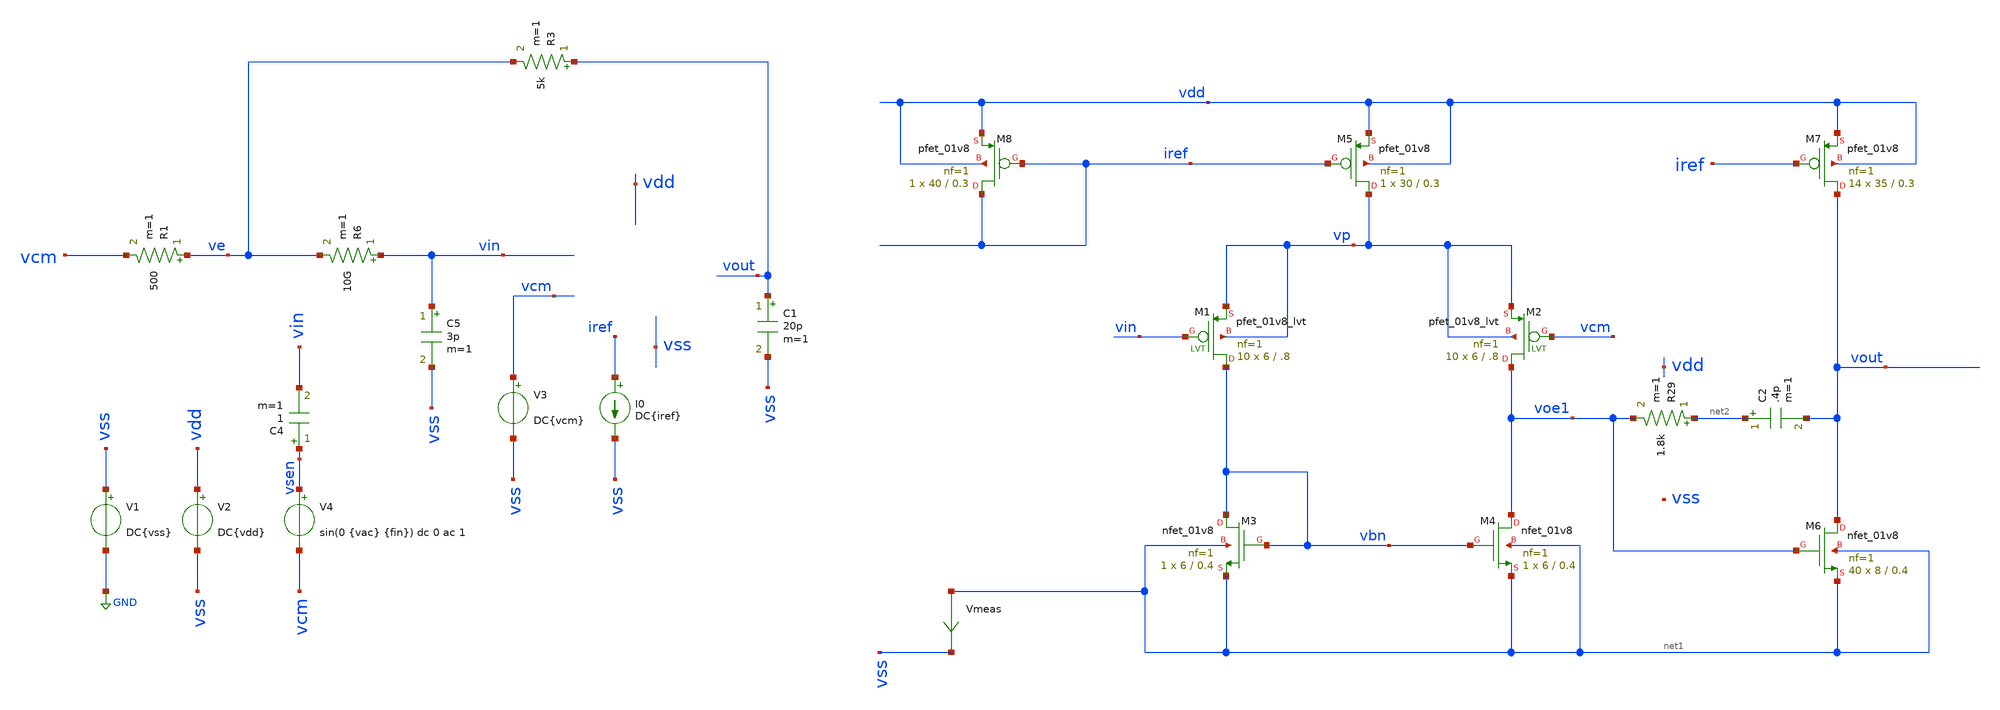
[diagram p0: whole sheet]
** sch_path: opamp/tb_opamp_openloop2.sch
**.subckt tb_opamp_openloop2
V1 vss GND DC{vss}
V2 vdd vss DC{vdd}
V3 vcm vss DC{vcm}
V4 vsen vcm sin(0 {vac} {fin}) dc 0 ac 1
C4 vsen vin 1 m=1
I0 iref vss DC{iref}
R1 ve vcm 500 m=1
R3 vout ve 5k m=1
C5 vin vss 3p m=1
C1 vout vss 20p m=1
R6 vin ve 10G m=1
XM3 vbn vbn net1 net1 sky130_fd_pr__nfet_01v8 L=0.4 W=6 nf=1 ad='W * 0.29' as='W * 0.29' pd='2 * (W + 0.29)'
+ ps='2 * (W + 0.29)' nrd='0.29 / W' nrs='0.29 / W' sa=0 sb=0 sd=0 mult=1 m=1
XM4 voe1 vbn net1 net1 sky130_fd_pr__nfet_01v8 L=0.4 W=6 nf=1 ad='W * 0.29' as='W * 0.29' pd='2 * (W + 0.29)'
+ ps='2 * (W + 0.29)' nrd='0.29 / W' nrs='0.29 / W' sa=0 sb=0 sd=0 mult=1 m=1
XM5 vp iref vdd vdd sky130_fd_pr__pfet_01v8 L=0.3 W=30 nf=1 ad='W * 0.29' as='W * 0.29' pd='2 * (W + 0.29)'
+ ps='2 * (W + 0.29)' nrd='0.29 / W' nrs='0.29 / W' sa=0 sb=0 sd=0 mult=1 m=1
XM7 vout iref vdd vdd sky130_fd_pr__pfet_01v8 L=0.3 W=35 nf=1 ad='W * 0.29' as='W * 0.29' pd='2 * (W + 0.29)'
+ ps='2 * (W + 0.29)' nrd='0.29 / W' nrs='0.29 / W' sa=0 sb=0 sd=0 mult=14 m=14
XM8 iref iref vdd vdd sky130_fd_pr__pfet_01v8 L=0.3 W=40 nf=1 ad='W * 0.29' as='W * 0.29' pd='2 * (W + 0.29)'
+ ps='2 * (W + 0.29)' nrd='0.29 / W' nrs='0.29 / W' sa=0 sb=0 sd=0 mult=1 m=1
XM6 vout voe1 net1 net1 sky130_fd_pr__nfet_01v8 L=0.4 W=8 nf=1 ad='W * 0.29' as='W * 0.29' pd='2 * (W + 0.29)'
+ ps='2 * (W + 0.29)' nrd='0.29 / W' nrs='0.29 / W' sa=0 sb=0 sd=0 mult=40 m=40
XM1 vbn vin vp vp sky130_fd_pr__pfet_01v8_lvt L=.8 W=6 nf=1 ad='int((nf+1)/2) * W/nf * 0.29' as='int((nf+2)/2) * W/nf * 0.29'
+ pd='2*int((nf+1)/2) * (W/nf + 0.29)' ps='2*int((nf+2)/2) * (W/nf + 0.29)' nrd='0.29 / W' nrs='0.29 / W'
+ sa=0 sb=0 sd=0 mult=10 m=10
XM2 voe1 vcm vp vp sky130_fd_pr__pfet_01v8_lvt L=.8 W=6 nf=1 ad='int((nf+1)/2) * W/nf * 0.29' as='int((nf+2)/2) * W/nf * 0.29'
+ pd='2*int((nf+1)/2) * (W/nf + 0.29)' ps='2*int((nf+2)/2) * (W/nf + 0.29)' nrd='0.29 / W' nrs='0.29 / W'
+ sa=0 sb=0 sd=0 mult=10 m=10
C2 net2 vout .4p m=1
Vmeas net1 vss 0
.save i(vmeas)
R29 net2 voe1 1.8k m=1
**** begin user architecture code




* Circuit Parameters
.param iref = 100u
.param vdd  = 1.8
.param vss  = 0.0
.param vcm  = 0.8
.param vac  = 10m
.param fin  = 9.765625e5
.options TEMP = 65.0

* Include Models
*.lib ~/skywater/skywater-pdk/libraries/sky130_fd_pr_ngspice/latest/models/corners/sky130.lib TT
*.lib /foss/pdks/sky130A/libs.tech/ngspice/sky130.lib.spice tt
.lib /foss/pdks/sky130A/libs.tech/ngspice/sky130.lib.spice.tt.red tt
* OP Parameters & Singals to save
.save all  @M.X1.XM1.msky130_fd_pr__pfet_01v8_lvt[id] @M.X1.XM1.msky130_fd_pr__pfet_01v8_lvt[vth] @M.X1.XM1.msky130_fd_pr__pfet_01v8_lvt[vgs] @M.X1.XM1.msky130_fd_pr__pfet_01v8_lvt[vds] @M.X1.XM1.msky130_fd_pr__pfet_01v8_lvt[vdsat] @M.X1.XM1.msky130_fd_pr__pfet_01v8_lvt[gm] @M.X1.XM1.msky130_fd_pr__pfet_01v8_lvt[gds]  @M.X1.XM2.msky130_fd_pr__pfet_01v8_lvt[id] @M.X1.XM2.msky130_fd_pr__pfet_01v8_lvt[vth] @M.X1.XM2.msky130_fd_pr__pfet_01v8_lvt[vgs] @M.X1.XM2.msky130_fd_pr__pfet_01v8_lvt[vds] @M.X1.XM2.msky130_fd_pr__pfet_01v8_lvt[vdsat] @M.X1.XM2.msky130_fd_pr__pfet_01v8_lvt[gm] @M.X1.XM2.msky130_fd_pr__pfet_01v8_lvt[gds]  @M.X1.XM3.msky130_fd_pr__nfet_01v8[id] @M.X1.XM3.msky130_fd_pr__nfet_01v8[vth] @M.X1.XM3.msky130_fd_pr__nfet_01v8[vgs] @M.X1.XM3.msky130_fd_pr__nfet_01v8[vds] @M.X1.XM3.msky130_fd_pr__nfet_01v8[vdsat] @M.X1.XM3.msky130_fd_pr__nfet_01v8[gm] @M.X1.XM3.msky130_fd_pr__nfet_01v8[gds]  @M.X1.XM4.msky130_fd_pr__nfet_01v8[id] @M.X1.XM4.msky130_fd_pr__nfet_01v8[vth] @M.X1.XM4.msky130_fd_pr__nfet_01v8[vgs] @M.X1.XM4.msky130_fd_pr__nfet_01v8[vds] @M.X1.XM4.msky130_fd_pr__nfet_01v8[vdsat] @M.X1.XM4.msky130_fd_pr__nfet_01v8[gm] @M.X1.XM4.msky130_fd_pr__nfet_01v8[gds]  @M.X1.XM5.msky130_fd_pr__pfet_01v8[id] @M.X1.XM5.msky130_fd_pr__pfet_01v8[vth] @M.X1.XM5.msky130_fd_pr__pfet_01v8[vgs] @M.X1.XM5.msky130_fd_pr__pfet_01v8[vds] @M.X1.XM5.msky130_fd_pr__pfet_01v8[vdsat] @M.X1.XM5.msky130_fd_pr__pfet_01v8[gm] @M.X1.XM5.msky130_fd_pr__pfet_01v8[gds]  @M.X1.XM6.msky130_fd_pr__nfet_01v8[id] @M.X1.XM6.msky130_fd_pr__nfet_01v8[vth] @M.X1.XM6.msky130_fd_pr__nfet_01v8[vgs] @M.X1.XM6.msky130_fd_pr__nfet_01v8[vds] @M.X1.XM6.msky130_fd_pr__nfet_01v8[vdsat] @M.X1.XM6.msky130_fd_pr__nfet_01v8[gm] @M.X1.XM6.msky130_fd_pr__nfet_01v8[gds]  @M.X1.XM7.msky130_fd_pr__pfet_01v8[id] @M.X1.XM7.msky130_fd_pr__pfet_01v8[vth] @M.X1.XM7.msky130_fd_pr__pfet_01v8[vgs] @M.X1.XM7.msky130_fd_pr__pfet_01v8[vds] @M.X1.XM7.msky130_fd_pr__pfet_01v8[vdsat] @M.X1.XM7.msky130_fd_pr__pfet_01v8[gm] @M.X1.XM7.msky130_fd_pr__pfet_01v8[gds]  @M.X1.XM8.msky130_fd_pr__pfet_01v8[id] @M.X1.XM8.msky130_fd_pr__pfet_01v8[vth] @M.X1.XM8.msky130_fd_pr__pfet_01v8[vgs] @M.X1.XM8.msky130_fd_pr__pfet_01v8[vds] @M.X1.XM8.msky130_fd_pr__pfet_01v8[vdsat] @M.X1.XM8.msky130_fd_pr__pfet_01v8[gm] @M.X1.XM8.msky130_fd_pr__pfet_01v8[gds]  @M.X1.XM9.msky130_fd_pr__nfet_01v8[id] @M.X1.XM9.msky130_fd_pr__nfet_01v8[vth] @M.X1.XM9.msky130_fd_pr__nfet_01v8[vgs] @M.X1.XM9.msky130_fd_pr__nfet_01v8[vds] @M.X1.XM9.msky130_fd_pr__nfet_01v8[vdsat] @M.X1.XM9.msky130_fd_pr__nfet_01v8[gm] @M.X1.XM9.msky130_fd_pr__nfet_01v8[gds]

*Simulation
.control
  set color0 = white

  ac dec 100 1 10G
  setplot ac1
  meas ac GBW when vdb(vout)=0
  meas ac DCG find vdb(vout) at=1
  meas ac PM find vp(vout) when vdb(vout)=0
  print PM*180/PI
  meas ac GM find vdb(vout) when vp(vout)=0
  plot vdb(vout) {vp(vout)*180/PI}
  plot vdb(voe1) {vp(voe1)*180/PI}
  write tb_opamp_openloop_ac2.raw

  reset
  op
  setplot op1
  unset filetype
  write tb_opamp_openloop2.raw
.endc

.end


**** end user architecture code
**.ends
.GLOBAL GND
.end
